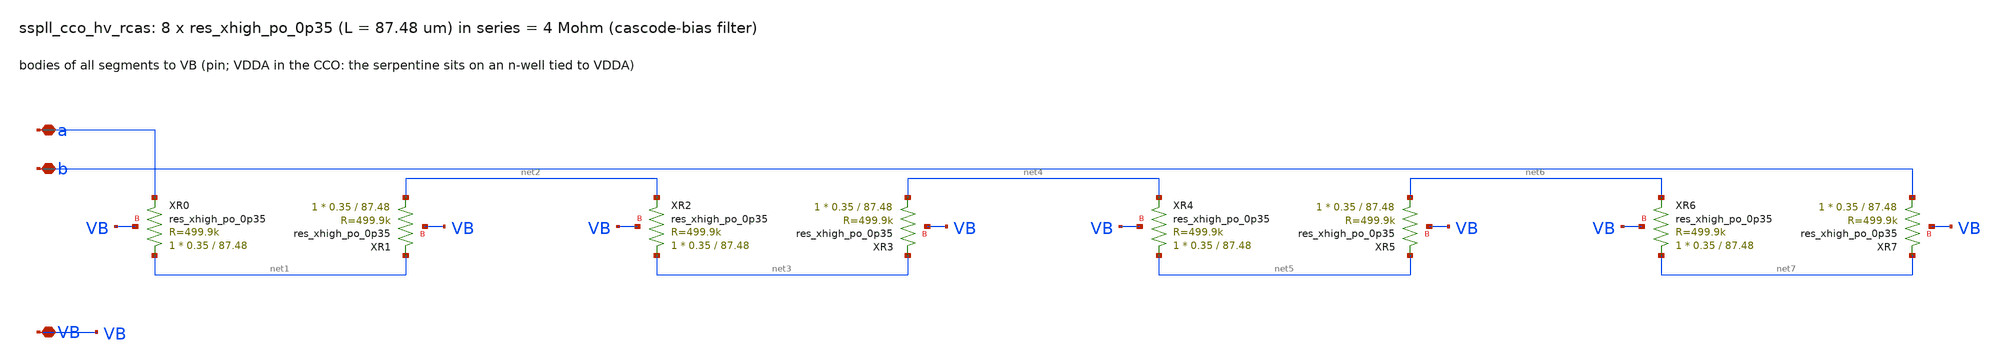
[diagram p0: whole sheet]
** sch_path: xschem/cco_hv/sspll_cco_hv_rcas.sch
**.subckt sspll_cco_hv_rcas a b VB
*.iopin a
*.iopin b
*.iopin VB
XXR0 net1 a VB sky130_fd_pr__res_xhigh_po_0p35 L=87.48 mult=1 m=1
XXR1 net2 net1 VB sky130_fd_pr__res_xhigh_po_0p35 L=87.48 mult=1 m=1
XXR2 net3 net2 VB sky130_fd_pr__res_xhigh_po_0p35 L=87.48 mult=1 m=1
XXR3 net4 net3 VB sky130_fd_pr__res_xhigh_po_0p35 L=87.48 mult=1 m=1
XXR4 net5 net4 VB sky130_fd_pr__res_xhigh_po_0p35 L=87.48 mult=1 m=1
XXR5 net6 net5 VB sky130_fd_pr__res_xhigh_po_0p35 L=87.48 mult=1 m=1
XXR6 net7 net6 VB sky130_fd_pr__res_xhigh_po_0p35 L=87.48 mult=1 m=1
XXR7 b net7 VB sky130_fd_pr__res_xhigh_po_0p35 L=87.48 mult=1 m=1
**.ends
.end
